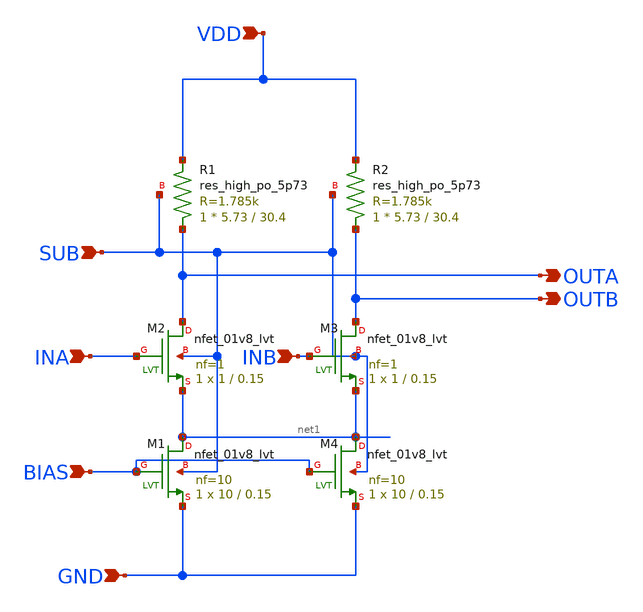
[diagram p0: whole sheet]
** sch_path: design/vco/5~10Ghiarachy_final/buffer_amp.sch
**.subckt buffer_amp INA INB BIAS GND VDD SUB OUTA OUTB
*.ipin INA
*.ipin INB
*.ipin BIAS
*.ipin GND
*.ipin VDD
*.ipin SUB
*.opin OUTA
*.opin OUTB
XM1 net1 BIAS GND SUB sky130_fd_pr__nfet_01v8_lvt L=0.15 W=10 nf=10 ad='int((nf+1)/2) * W/nf * 0.29'
+ as='int((nf+2)/2) * W/nf * 0.29' pd='2*int((nf+1)/2) * (W/nf + 0.29)' ps='2*int((nf+2)/2) * (W/nf + 0.29)'
+ nrd='0.29 / W' nrs='0.29 / W' sa=0 sb=0 sd=0 mult=1 m=1
XM2 OUTA INA net1 SUB sky130_fd_pr__nfet_01v8_lvt L=0.15 W=1 nf=1 ad='int((nf+1)/2) * W/nf * 0.29' as='int((nf+2)/2) * W/nf * 0.29'
+ pd='2*int((nf+1)/2) * (W/nf + 0.29)' ps='2*int((nf+2)/2) * (W/nf + 0.29)' nrd='0.29 / W' nrs='0.29 / W'
+ sa=0 sb=0 sd=0 mult=1 m=1
XM3 OUTB INB net1 SUB sky130_fd_pr__nfet_01v8_lvt L=0.15 W=1 nf=1 ad='int((nf+1)/2) * W/nf * 0.29' as='int((nf+2)/2) * W/nf * 0.29'
+ pd='2*int((nf+1)/2) * (W/nf + 0.29)' ps='2*int((nf+2)/2) * (W/nf + 0.29)' nrd='0.29 / W' nrs='0.29 / W'
+ sa=0 sb=0 sd=0 mult=1 m=1
XR2 OUTB VDD SUB sky130_fd_pr__res_high_po_5p73 L=30.4 mult=1 m=1
XR1 OUTA VDD SUB sky130_fd_pr__res_high_po_5p73 L=30.4 mult=1 m=1
XM4 net1 BIAS GND SUB sky130_fd_pr__nfet_01v8_lvt L=0.15 W=10 nf=10 ad='int((nf+1)/2) * W/nf * 0.29'
+ as='int((nf+2)/2) * W/nf * 0.29' pd='2*int((nf+1)/2) * (W/nf + 0.29)' ps='2*int((nf+2)/2) * (W/nf + 0.29)'
+ nrd='0.29 / W' nrs='0.29 / W' sa=0 sb=0 sd=0 mult=1 m=1
**.ends
.end
